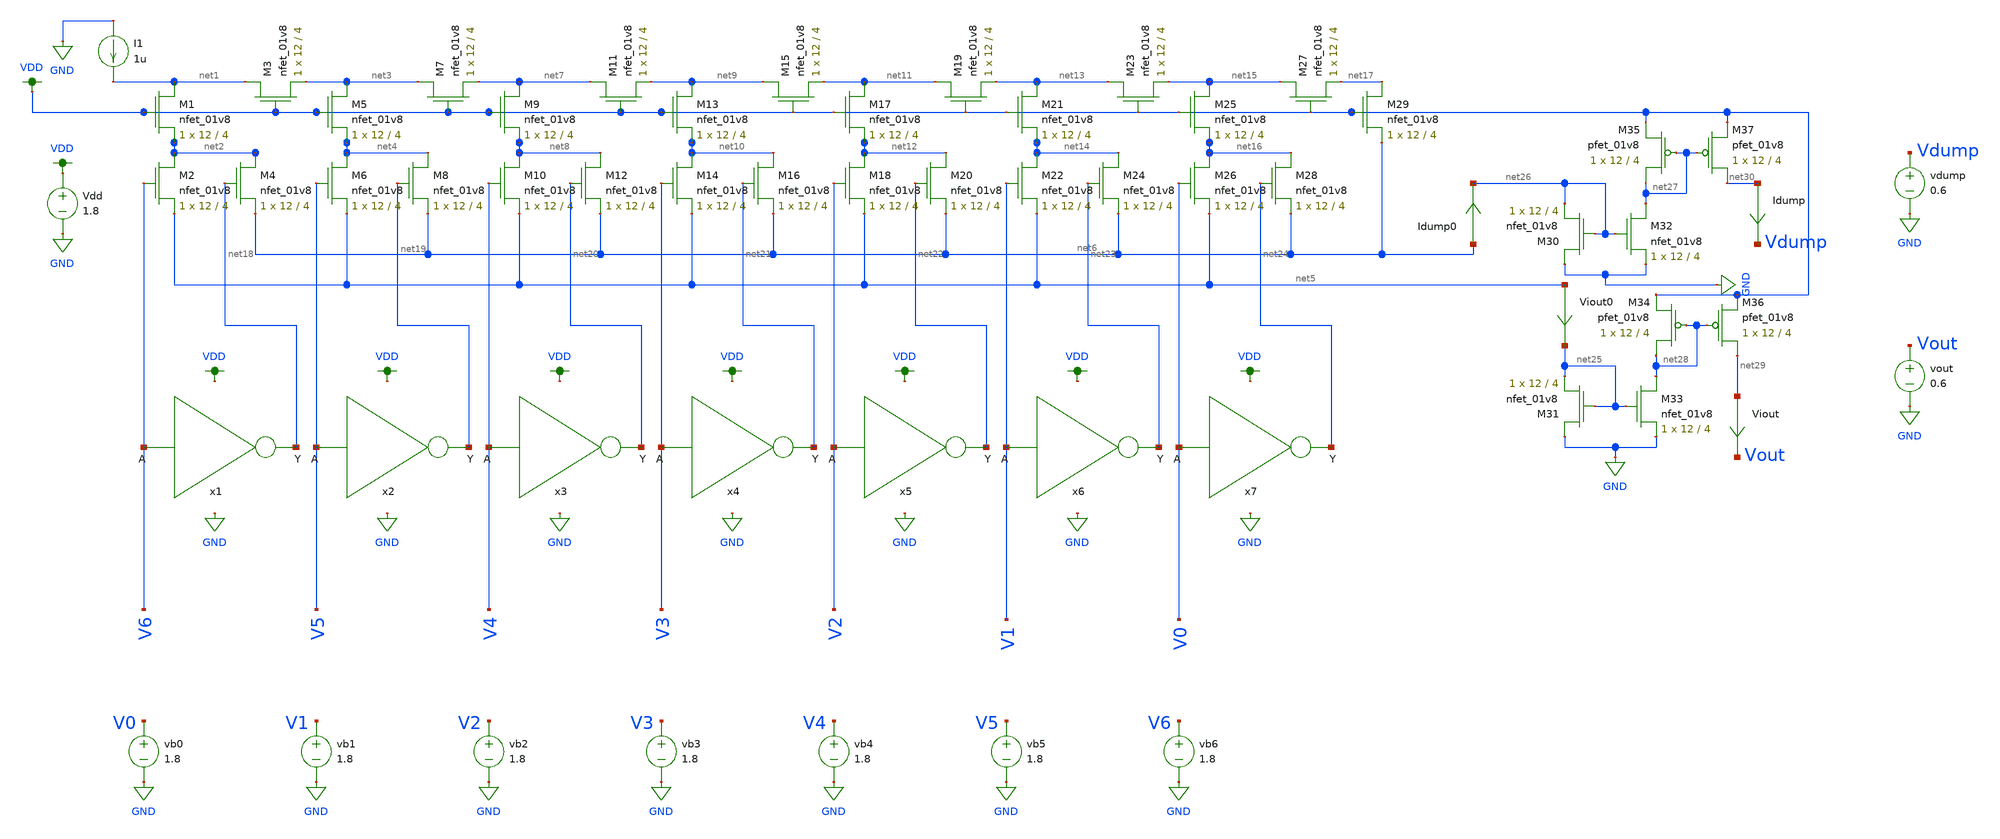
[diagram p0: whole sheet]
** sch_path: xschem/ladder_dac_simulation.sch
**.subckt ladder_dac_simulation
XM1 net1 VDD net2 GND sky130_fd_pr__nfet_01v8 L=4 W=12 nf=1 ad='int((nf+1)/2) * W/nf * 0.29' as='int((nf+2)/2) * W/nf * 0.29'
+ pd='2*int((nf+1)/2) * (W/nf + 0.29)' ps='2*int((nf+2)/2) * (W/nf + 0.29)' nrd='0.29 / W' nrs='0.29 / W'
+ sa=0 sb=0 sd=0 mult=1 m=1
XM3 net1 VDD net3 GND sky130_fd_pr__nfet_01v8 L=4 W=12 nf=1 ad='int((nf+1)/2) * W/nf * 0.29' as='int((nf+2)/2) * W/nf * 0.29'
+ pd='2*int((nf+1)/2) * (W/nf + 0.29)' ps='2*int((nf+2)/2) * (W/nf + 0.29)' nrd='0.29 / W' nrs='0.29 / W'
+ sa=0 sb=0 sd=0 mult=1 m=1
XM5 net3 VDD net4 GND sky130_fd_pr__nfet_01v8 L=4 W=12 nf=1 ad='int((nf+1)/2) * W/nf * 0.29' as='int((nf+2)/2) * W/nf * 0.29'
+ pd='2*int((nf+1)/2) * (W/nf + 0.29)' ps='2*int((nf+2)/2) * (W/nf + 0.29)' nrd='0.29 / W' nrs='0.29 / W'
+ sa=0 sb=0 sd=0 mult=1 m=1
XM7 net3 VDD net7 GND sky130_fd_pr__nfet_01v8 L=4 W=12 nf=1 ad='int((nf+1)/2) * W/nf * 0.29' as='int((nf+2)/2) * W/nf * 0.29'
+ pd='2*int((nf+1)/2) * (W/nf + 0.29)' ps='2*int((nf+2)/2) * (W/nf + 0.29)' nrd='0.29 / W' nrs='0.29 / W'
+ sa=0 sb=0 sd=0 mult=1 m=1
XM6 net4 V5 net5 GND sky130_fd_pr__nfet_01v8 L=4 W=12 nf=1 ad='int((nf+1)/2) * W/nf * 0.29' as='int((nf+2)/2) * W/nf * 0.29'
+ pd='2*int((nf+1)/2) * (W/nf + 0.29)' ps='2*int((nf+2)/2) * (W/nf + 0.29)' nrd='0.29 / W' nrs='0.29 / W'
+ sa=0 sb=0 sd=0 mult=1 m=1
XM8 net4 net19 net6 GND sky130_fd_pr__nfet_01v8 L=4 W=12 nf=1 ad='int((nf+1)/2) * W/nf * 0.29' as='int((nf+2)/2) * W/nf * 0.29'
+ pd='2*int((nf+1)/2) * (W/nf + 0.29)' ps='2*int((nf+2)/2) * (W/nf + 0.29)' nrd='0.29 / W' nrs='0.29 / W'
+ sa=0 sb=0 sd=0 mult=1 m=1
XM2 net2 V6 net5 GND sky130_fd_pr__nfet_01v8 L=4 W=12 nf=1 ad='int((nf+1)/2) * W/nf * 0.29' as='int((nf+2)/2) * W/nf * 0.29'
+ pd='2*int((nf+1)/2) * (W/nf + 0.29)' ps='2*int((nf+2)/2) * (W/nf + 0.29)' nrd='0.29 / W' nrs='0.29 / W'
+ sa=0 sb=0 sd=0 mult=1 m=1
XM4 net2 net18 net6 GND sky130_fd_pr__nfet_01v8 L=4 W=12 nf=1 ad='int((nf+1)/2) * W/nf * 0.29' as='int((nf+2)/2) * W/nf * 0.29'
+ pd='2*int((nf+1)/2) * (W/nf + 0.29)' ps='2*int((nf+2)/2) * (W/nf + 0.29)' nrd='0.29 / W' nrs='0.29 / W'
+ sa=0 sb=0 sd=0 mult=1 m=1
XM9 net7 VDD net8 GND sky130_fd_pr__nfet_01v8 L=4 W=12 nf=1 ad='int((nf+1)/2) * W/nf * 0.29' as='int((nf+2)/2) * W/nf * 0.29'
+ pd='2*int((nf+1)/2) * (W/nf + 0.29)' ps='2*int((nf+2)/2) * (W/nf + 0.29)' nrd='0.29 / W' nrs='0.29 / W'
+ sa=0 sb=0 sd=0 mult=1 m=1
XM11 net7 VDD net9 GND sky130_fd_pr__nfet_01v8 L=4 W=12 nf=1 ad='int((nf+1)/2) * W/nf * 0.29' as='int((nf+2)/2) * W/nf * 0.29'
+ pd='2*int((nf+1)/2) * (W/nf + 0.29)' ps='2*int((nf+2)/2) * (W/nf + 0.29)' nrd='0.29 / W' nrs='0.29 / W'
+ sa=0 sb=0 sd=0 mult=1 m=1
XM10 net8 V4 net5 GND sky130_fd_pr__nfet_01v8 L=4 W=12 nf=1 ad='int((nf+1)/2) * W/nf * 0.29' as='int((nf+2)/2) * W/nf * 0.29'
+ pd='2*int((nf+1)/2) * (W/nf + 0.29)' ps='2*int((nf+2)/2) * (W/nf + 0.29)' nrd='0.29 / W' nrs='0.29 / W'
+ sa=0 sb=0 sd=0 mult=1 m=1
XM12 net8 net20 net6 GND sky130_fd_pr__nfet_01v8 L=4 W=12 nf=1 ad='int((nf+1)/2) * W/nf * 0.29' as='int((nf+2)/2) * W/nf * 0.29'
+ pd='2*int((nf+1)/2) * (W/nf + 0.29)' ps='2*int((nf+2)/2) * (W/nf + 0.29)' nrd='0.29 / W' nrs='0.29 / W'
+ sa=0 sb=0 sd=0 mult=1 m=1
XM13 net9 VDD net10 GND sky130_fd_pr__nfet_01v8 L=4 W=12 nf=1 ad='int((nf+1)/2) * W/nf * 0.29' as='int((nf+2)/2) * W/nf * 0.29'
+ pd='2*int((nf+1)/2) * (W/nf + 0.29)' ps='2*int((nf+2)/2) * (W/nf + 0.29)' nrd='0.29 / W' nrs='0.29 / W'
+ sa=0 sb=0 sd=0 mult=1 m=1
XM15 net9 VDD net11 GND sky130_fd_pr__nfet_01v8 L=4 W=12 nf=1 ad='int((nf+1)/2) * W/nf * 0.29' as='int((nf+2)/2) * W/nf * 0.29'
+ pd='2*int((nf+1)/2) * (W/nf + 0.29)' ps='2*int((nf+2)/2) * (W/nf + 0.29)' nrd='0.29 / W' nrs='0.29 / W'
+ sa=0 sb=0 sd=0 mult=1 m=1
XM14 net10 V3 net5 GND sky130_fd_pr__nfet_01v8 L=4 W=12 nf=1 ad='int((nf+1)/2) * W/nf * 0.29' as='int((nf+2)/2) * W/nf * 0.29'
+ pd='2*int((nf+1)/2) * (W/nf + 0.29)' ps='2*int((nf+2)/2) * (W/nf + 0.29)' nrd='0.29 / W' nrs='0.29 / W'
+ sa=0 sb=0 sd=0 mult=1 m=1
XM16 net10 net21 net6 GND sky130_fd_pr__nfet_01v8 L=4 W=12 nf=1 ad='int((nf+1)/2) * W/nf * 0.29' as='int((nf+2)/2) * W/nf * 0.29'
+ pd='2*int((nf+1)/2) * (W/nf + 0.29)' ps='2*int((nf+2)/2) * (W/nf + 0.29)' nrd='0.29 / W' nrs='0.29 / W'
+ sa=0 sb=0 sd=0 mult=1 m=1
XM17 net11 VDD net12 GND sky130_fd_pr__nfet_01v8 L=4 W=12 nf=1 ad='int((nf+1)/2) * W/nf * 0.29' as='int((nf+2)/2) * W/nf * 0.29'
+ pd='2*int((nf+1)/2) * (W/nf + 0.29)' ps='2*int((nf+2)/2) * (W/nf + 0.29)' nrd='0.29 / W' nrs='0.29 / W'
+ sa=0 sb=0 sd=0 mult=1 m=1
XM19 net11 VDD net13 GND sky130_fd_pr__nfet_01v8 L=4 W=12 nf=1 ad='int((nf+1)/2) * W/nf * 0.29' as='int((nf+2)/2) * W/nf * 0.29'
+ pd='2*int((nf+1)/2) * (W/nf + 0.29)' ps='2*int((nf+2)/2) * (W/nf + 0.29)' nrd='0.29 / W' nrs='0.29 / W'
+ sa=0 sb=0 sd=0 mult=1 m=1
XM18 net12 V2 net5 GND sky130_fd_pr__nfet_01v8 L=4 W=12 nf=1 ad='int((nf+1)/2) * W/nf * 0.29' as='int((nf+2)/2) * W/nf * 0.29'
+ pd='2*int((nf+1)/2) * (W/nf + 0.29)' ps='2*int((nf+2)/2) * (W/nf + 0.29)' nrd='0.29 / W' nrs='0.29 / W'
+ sa=0 sb=0 sd=0 mult=1 m=1
XM20 net12 net22 net6 GND sky130_fd_pr__nfet_01v8 L=4 W=12 nf=1 ad='int((nf+1)/2) * W/nf * 0.29' as='int((nf+2)/2) * W/nf * 0.29'
+ pd='2*int((nf+1)/2) * (W/nf + 0.29)' ps='2*int((nf+2)/2) * (W/nf + 0.29)' nrd='0.29 / W' nrs='0.29 / W'
+ sa=0 sb=0 sd=0 mult=1 m=1
XM21 net13 VDD net14 GND sky130_fd_pr__nfet_01v8 L=4 W=12 nf=1 ad='int((nf+1)/2) * W/nf * 0.29' as='int((nf+2)/2) * W/nf * 0.29'
+ pd='2*int((nf+1)/2) * (W/nf + 0.29)' ps='2*int((nf+2)/2) * (W/nf + 0.29)' nrd='0.29 / W' nrs='0.29 / W'
+ sa=0 sb=0 sd=0 mult=1 m=1
XM23 net13 VDD net15 GND sky130_fd_pr__nfet_01v8 L=4 W=12 nf=1 ad='int((nf+1)/2) * W/nf * 0.29' as='int((nf+2)/2) * W/nf * 0.29'
+ pd='2*int((nf+1)/2) * (W/nf + 0.29)' ps='2*int((nf+2)/2) * (W/nf + 0.29)' nrd='0.29 / W' nrs='0.29 / W'
+ sa=0 sb=0 sd=0 mult=1 m=1
XM22 net14 V1 net5 GND sky130_fd_pr__nfet_01v8 L=4 W=12 nf=1 ad='int((nf+1)/2) * W/nf * 0.29' as='int((nf+2)/2) * W/nf * 0.29'
+ pd='2*int((nf+1)/2) * (W/nf + 0.29)' ps='2*int((nf+2)/2) * (W/nf + 0.29)' nrd='0.29 / W' nrs='0.29 / W'
+ sa=0 sb=0 sd=0 mult=1 m=1
XM24 net14 net23 net6 GND sky130_fd_pr__nfet_01v8 L=4 W=12 nf=1 ad='int((nf+1)/2) * W/nf * 0.29' as='int((nf+2)/2) * W/nf * 0.29'
+ pd='2*int((nf+1)/2) * (W/nf + 0.29)' ps='2*int((nf+2)/2) * (W/nf + 0.29)' nrd='0.29 / W' nrs='0.29 / W'
+ sa=0 sb=0 sd=0 mult=1 m=1
XM25 net15 VDD net16 GND sky130_fd_pr__nfet_01v8 L=4 W=12 nf=1 ad='int((nf+1)/2) * W/nf * 0.29' as='int((nf+2)/2) * W/nf * 0.29'
+ pd='2*int((nf+1)/2) * (W/nf + 0.29)' ps='2*int((nf+2)/2) * (W/nf + 0.29)' nrd='0.29 / W' nrs='0.29 / W'
+ sa=0 sb=0 sd=0 mult=1 m=1
XM27 net15 VDD net17 GND sky130_fd_pr__nfet_01v8 L=4 W=12 nf=1 ad='int((nf+1)/2) * W/nf * 0.29' as='int((nf+2)/2) * W/nf * 0.29'
+ pd='2*int((nf+1)/2) * (W/nf + 0.29)' ps='2*int((nf+2)/2) * (W/nf + 0.29)' nrd='0.29 / W' nrs='0.29 / W'
+ sa=0 sb=0 sd=0 mult=1 m=1
XM26 net16 V0 net5 GND sky130_fd_pr__nfet_01v8 L=4 W=12 nf=1 ad='int((nf+1)/2) * W/nf * 0.29' as='int((nf+2)/2) * W/nf * 0.29'
+ pd='2*int((nf+1)/2) * (W/nf + 0.29)' ps='2*int((nf+2)/2) * (W/nf + 0.29)' nrd='0.29 / W' nrs='0.29 / W'
+ sa=0 sb=0 sd=0 mult=1 m=1
XM28 net16 net24 net6 GND sky130_fd_pr__nfet_01v8 L=4 W=12 nf=1 ad='int((nf+1)/2) * W/nf * 0.29' as='int((nf+2)/2) * W/nf * 0.29'
+ pd='2*int((nf+1)/2) * (W/nf + 0.29)' ps='2*int((nf+2)/2) * (W/nf + 0.29)' nrd='0.29 / W' nrs='0.29 / W'
+ sa=0 sb=0 sd=0 mult=1 m=1
XM29 net17 VDD net6 GND sky130_fd_pr__nfet_01v8 L=4 W=12 nf=1 ad='int((nf+1)/2) * W/nf * 0.29' as='int((nf+2)/2) * W/nf * 0.29'
+ pd='2*int((nf+1)/2) * (W/nf + 0.29)' ps='2*int((nf+2)/2) * (W/nf + 0.29)' nrd='0.29 / W' nrs='0.29 / W'
+ sa=0 sb=0 sd=0 mult=1 m=1
x1 net18 V6 inverter
x2 net19 V5 inverter
x3 net20 V4 inverter
x4 net21 V3 inverter
x5 net22 V2 inverter
x6 net23 V1 inverter
x7 net24 V0 inverter
XM30 GND net26 net26 GND sky130_fd_pr__nfet_01v8 L=4 W=12 nf=1 ad='int((nf+1)/2) * W/nf * 0.29' as='int((nf+2)/2) * W/nf * 0.29'
+ pd='2*int((nf+1)/2) * (W/nf + 0.29)' ps='2*int((nf+2)/2) * (W/nf + 0.29)' nrd='0.29 / W' nrs='0.29 / W'
+ sa=0 sb=0 sd=0 mult=1 m=1
XM31 GND net25 net25 GND sky130_fd_pr__nfet_01v8 L=4 W=12 nf=1 ad='int((nf+1)/2) * W/nf * 0.29' as='int((nf+2)/2) * W/nf * 0.29'
+ pd='2*int((nf+1)/2) * (W/nf + 0.29)' ps='2*int((nf+2)/2) * (W/nf + 0.29)' nrd='0.29 / W' nrs='0.29 / W'
+ sa=0 sb=0 sd=0 mult=1 m=1
XM32 net27 net26 GND GND sky130_fd_pr__nfet_01v8 L=4 W=12 nf=1 ad='int((nf+1)/2) * W/nf * 0.29' as='int((nf+2)/2) * W/nf * 0.29'
+ pd='2*int((nf+1)/2) * (W/nf + 0.29)' ps='2*int((nf+2)/2) * (W/nf + 0.29)' nrd='0.29 / W' nrs='0.29 / W'
+ sa=0 sb=0 sd=0 mult=1 m=1
XM33 net28 net25 GND GND sky130_fd_pr__nfet_01v8 L=4 W=12 nf=1 ad='int((nf+1)/2) * W/nf * 0.29' as='int((nf+2)/2) * W/nf * 0.29'
+ pd='2*int((nf+1)/2) * (W/nf + 0.29)' ps='2*int((nf+2)/2) * (W/nf + 0.29)' nrd='0.29 / W' nrs='0.29 / W'
+ sa=0 sb=0 sd=0 mult=1 m=1
XM35 net27 net27 VDD VDD sky130_fd_pr__pfet_01v8 L=4 W=12 nf=1 ad='int((nf+1)/2) * W/nf * 0.29' as='int((nf+2)/2) * W/nf * 0.29'
+ pd='2*int((nf+1)/2) * (W/nf + 0.29)' ps='2*int((nf+2)/2) * (W/nf + 0.29)' nrd='0.29 / W' nrs='0.29 / W'
+ sa=0 sb=0 sd=0 mult=1 m=1
XM37 net30 net27 VDD VDD sky130_fd_pr__pfet_01v8 L=4 W=12 nf=1 ad='int((nf+1)/2) * W/nf * 0.29' as='int((nf+2)/2) * W/nf * 0.29'
+ pd='2*int((nf+1)/2) * (W/nf + 0.29)' ps='2*int((nf+2)/2) * (W/nf + 0.29)' nrd='0.29 / W' nrs='0.29 / W'
+ sa=0 sb=0 sd=0 mult=1 m=1
XM34 net28 net28 VDD VDD sky130_fd_pr__pfet_01v8 L=4 W=12 nf=1 ad='int((nf+1)/2) * W/nf * 0.29' as='int((nf+2)/2) * W/nf * 0.29'
+ pd='2*int((nf+1)/2) * (W/nf + 0.29)' ps='2*int((nf+2)/2) * (W/nf + 0.29)' nrd='0.29 / W' nrs='0.29 / W'
+ sa=0 sb=0 sd=0 mult=1 m=1
XM36 net29 net28 VDD VDD sky130_fd_pr__pfet_01v8 L=4 W=12 nf=1 ad='int((nf+1)/2) * W/nf * 0.29' as='int((nf+2)/2) * W/nf * 0.29'
+ pd='2*int((nf+1)/2) * (W/nf + 0.29)' ps='2*int((nf+2)/2) * (W/nf + 0.29)' nrd='0.29 / W' nrs='0.29 / W'
+ sa=0 sb=0 sd=0 mult=1 m=1
I1 GND net1 1u
Vdd VDD GND 1.8
vb0 V0 GND 1.8
vb1 V1 GND 1.8
vb2 V2 GND 1.8
vb3 V3 GND 1.8
vb4 V4 GND 1.8
vb5 V5 GND 1.8
vb6 V6 GND 1.8
vdump Vdump GND 0.6
vout Vout GND 0.6
Idump net30 Vdump 0
.save i(idump)
Viout net29 Vout 0
.save i(viout)
Idump0 net6 net26 0
.save i(idump0)
Viout0 net5 net25 0
.save i(viout0)
**** begin user architecture code

.option wnflag=1
.param MC_SWITCH=0.0
.lib ~/skywater/skywater-pdk/libraries/sky130_fd_pr_ngspice/latest/models/sky130.lib.spice tt



.control
  set wr_vecnames
  set wr_singlescale
  let code = 0
  while code < 128
    if code eq 0
      let b0 = 0
    else
      let b0 = code % 2
    end
    if floor(code / 2) eq 0
      let b1 = 0
    else
      let b1 = floor(code / 2) % 2
    end
    if floor(code / 4) eq 0
      let b2 = 0
    else
      let b2 = floor(code / 4) % 2
    end
    if floor(code / 8) eq 0
      let b3 = 0
    else
      let b3 = floor(code / 8) % 2
    end
    if floor(code / 16) eq 0
      let b4 = 0
    else
      let b4 = floor(code / 16) % 2
    end
    if floor(code / 32) eq 0
      let b5 = 0
    else
      let b5 = floor(code / 32) % 2
    end
    if floor(code / 64) eq 0
      let b6 = 0
    else
      let b6 = floor(code / 64) % 2
    end
    alter Vb0 1.8*$&b0
    alter Vb1 1.8*$&b1
    alter Vb2 1.8*$&b2
    alter Vb3 1.8*$&b3
    alter Vb4 1.8*$&b4
    alter Vb5 1.8*$&b5
    alter Vb6 1.8*$&b6
    save all
    op
    wrdata ~/Documents/DAC-VLSI/simulation_results/ladder_dac_simulation_andrew.txt v(b0) v(b1)
+ v(b2) v(b3) v(b4) v(b5) v(b6) i(Viout0)
    if code eq 0
      set appendwrite
      set wr_vecnames = FALSE
    end
    let code = code + 1
  end
  quit
.endc

**** end user architecture code
**.ends

* expanding   symbol:  ./inverter.sym # of pins=2
** sym_path: xschem/inverter.sym
** sch_path: xschem/inverter.sch
.subckt inverter Y A
*.ipin A
*.opin Y
XM1 Y A VDD VDD sky130_fd_pr__pfet_01v8 L=0.15 W=1 nf=1 ad='int((nf+1)/2) * W/nf * 0.29' as='int((nf+2)/2) * W/nf * 0.29'
+ pd='2*int((nf+1)/2) * (W/nf + 0.29)' ps='2*int((nf+2)/2) * (W/nf + 0.29)' nrd='0.29 / W' nrs='0.29 / W'
+ sa=0 sb=0 sd=0 mult=1 m=1
XM2 Y A GND GND sky130_fd_pr__nfet_01v8 L=0.15 W=1 nf=1 ad='int((nf+1)/2) * W/nf * 0.29' as='int((nf+2)/2) * W/nf * 0.29'
+ pd='2*int((nf+1)/2) * (W/nf + 0.29)' ps='2*int((nf+2)/2) * (W/nf + 0.29)' nrd='0.29 / W' nrs='0.29 / W'
+ sa=0 sb=0 sd=0 mult=1 m=1
.ends

.GLOBAL VDD
.GLOBAL GND
.end
